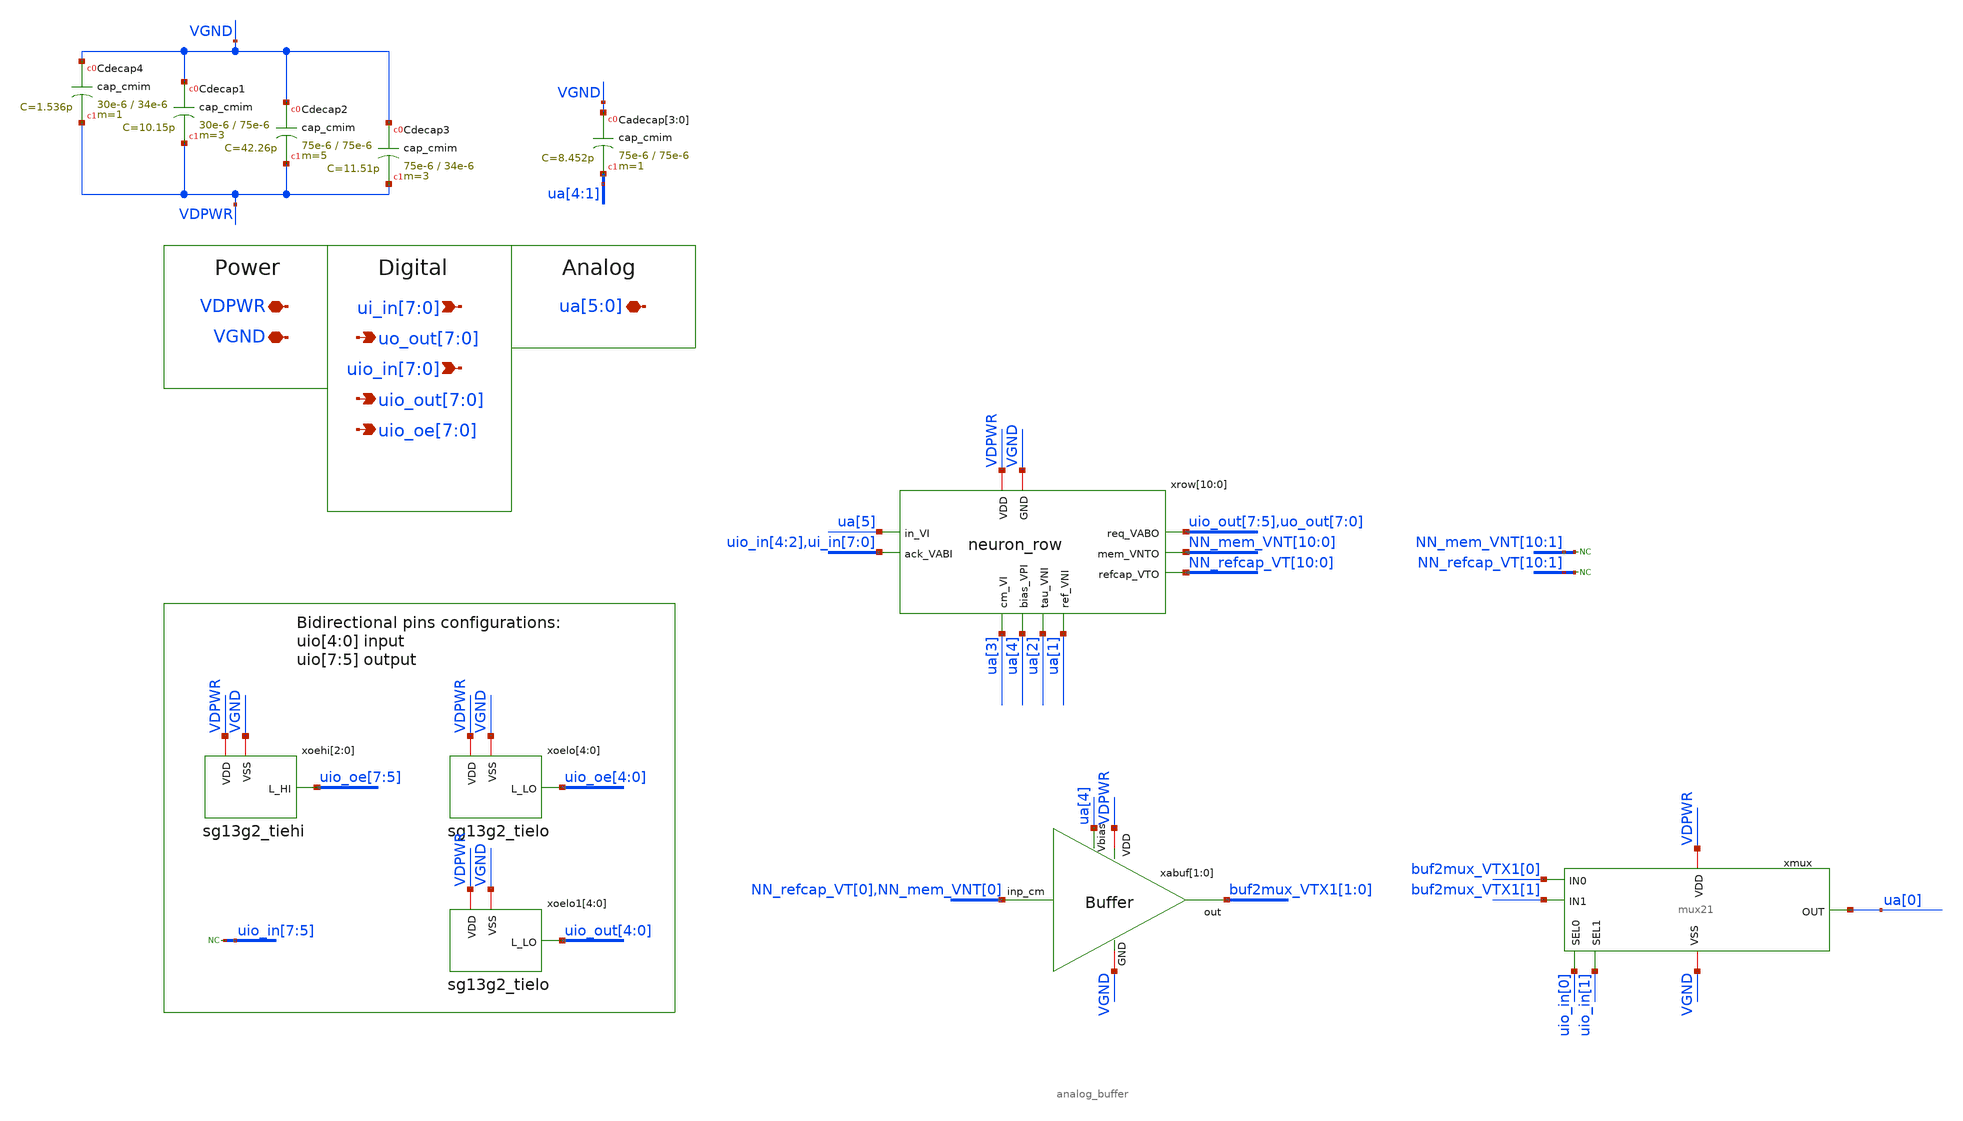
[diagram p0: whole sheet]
** sch_path: xschem/chip_top.sch
**.subckt chip_top VDPWR VGND
*+ ui_in[7],ui_in[6],ui_in[5],ui_in[4],ui_in[3],ui_in[2],ui_in[1],ui_in[0] uo_out[7],uo_out[6],uo_out[5],uo_out[4],uo_out[3],uo_out[2],uo_out[1],uo_out[0]
*+ uio_in[7],uio_in[6],uio_in[5],uio_in[4],uio_in[3],uio_in[2],uio_in[1],uio_in[0] uio_out[7],uio_out[6],uio_out[5],uio_out[4],uio_out[3],uio_out[2],uio_out[1],uio_out[0]
*+ uio_oe[7],uio_oe[6],uio_oe[5],uio_oe[4],uio_oe[3],uio_oe[2],uio_oe[1],uio_oe[0] ua[5],ua[4],ua[3],ua[2],ua[1],ua[0]
*.iopin VDPWR
*.iopin VGND
*.ipin ui_in[7],ui_in[6],ui_in[5],ui_in[4],ui_in[3],ui_in[2],ui_in[1],ui_in[0]
*.opin uo_out[7],uo_out[6],uo_out[5],uo_out[4],uo_out[3],uo_out[2],uo_out[1],uo_out[0]
*.ipin uio_in[7],uio_in[6],uio_in[5],uio_in[4],uio_in[3],uio_in[2],uio_in[1],uio_in[0]
*.opin uio_out[7],uio_out[6],uio_out[5],uio_out[4],uio_out[3],uio_out[2],uio_out[1],uio_out[0]
*.opin uio_oe[7],uio_oe[6],uio_oe[5],uio_oe[4],uio_oe[3],uio_oe[2],uio_oe[1],uio_oe[0]
*.iopin ua[5],ua[4],ua[3],ua[2],ua[1],ua[0]
xrow[10] VDPWR VGND ua[4] ua[5] NN_mem_VNT[10] ua[3] ua[2] uio_out[7] ua[1] NN_refcap_VT[10]
+ uio_in[4] neuron_row
xrow[9] VDPWR VGND ua[4] ua[5] NN_mem_VNT[9] ua[3] ua[2] uio_out[6] ua[1] NN_refcap_VT[9] uio_in[3]
+ neuron_row
xrow[8] VDPWR VGND ua[4] ua[5] NN_mem_VNT[8] ua[3] ua[2] uio_out[5] ua[1] NN_refcap_VT[8] uio_in[2]
+ neuron_row
xrow[7] VDPWR VGND ua[4] ua[5] NN_mem_VNT[7] ua[3] ua[2] uo_out[7] ua[1] NN_refcap_VT[7] ui_in[7]
+ neuron_row
xrow[6] VDPWR VGND ua[4] ua[5] NN_mem_VNT[6] ua[3] ua[2] uo_out[6] ua[1] NN_refcap_VT[6] ui_in[6]
+ neuron_row
xrow[5] VDPWR VGND ua[4] ua[5] NN_mem_VNT[5] ua[3] ua[2] uo_out[5] ua[1] NN_refcap_VT[5] ui_in[5]
+ neuron_row
xrow[4] VDPWR VGND ua[4] ua[5] NN_mem_VNT[4] ua[3] ua[2] uo_out[4] ua[1] NN_refcap_VT[4] ui_in[4]
+ neuron_row
xrow[3] VDPWR VGND ua[4] ua[5] NN_mem_VNT[3] ua[3] ua[2] uo_out[3] ua[1] NN_refcap_VT[3] ui_in[3]
+ neuron_row
xrow[2] VDPWR VGND ua[4] ua[5] NN_mem_VNT[2] ua[3] ua[2] uo_out[2] ua[1] NN_refcap_VT[2] ui_in[2]
+ neuron_row
xrow[1] VDPWR VGND ua[4] ua[5] NN_mem_VNT[1] ua[3] ua[2] uo_out[1] ua[1] NN_refcap_VT[1] ui_in[1]
+ neuron_row
xrow[0] VDPWR VGND ua[4] ua[5] NN_mem_VNT[0] ua[3] ua[2] uo_out[0] ua[1] NN_refcap_VT[0] ui_in[0]
+ neuron_row
xabuf[1] NN_refcap_VT[0] VDPWR ua[4] buf2mux_VTX1[1] VGND analog_buffer
xabuf[0] NN_mem_VNT[0] VDPWR ua[4] buf2mux_VTX1[0] VGND analog_buffer
xmux VDPWR VGND buf2mux_VTX1[0] buf2mux_VTX1[1] uio_in[0] uio_in[1] ua[0] mux21
xoehi[2] VDPWR VGND uio_oe[7] sg13g2_tiehi
xoehi[1] VDPWR VGND uio_oe[6] sg13g2_tiehi
xoehi[0] VDPWR VGND uio_oe[5] sg13g2_tiehi
xoelo[4] VDPWR VGND uio_oe[4] sg13g2_tielo
xoelo[3] VDPWR VGND uio_oe[3] sg13g2_tielo
xoelo[2] VDPWR VGND uio_oe[2] sg13g2_tielo
xoelo[1] VDPWR VGND uio_oe[1] sg13g2_tielo
xoelo[0] VDPWR VGND uio_oe[0] sg13g2_tielo
xoelo1[4] VDPWR VGND uio_out[4] sg13g2_tielo
xoelo1[3] VDPWR VGND uio_out[3] sg13g2_tielo
xoelo1[2] VDPWR VGND uio_out[2] sg13g2_tielo
xoelo1[1] VDPWR VGND uio_out[1] sg13g2_tielo
xoelo1[0] VDPWR VGND uio_out[0] sg13g2_tielo
* noconn uio_in[7:5]
* noconn NN_mem_VNT[10:1]
* noconn NN_refcap_VT[10:1]
XCadecap[3] VGND ua[4] cap_cmim w=75e-6 l=75e-6 m=1 mm_ok=1
XCadecap[2] VGND ua[3] cap_cmim w=75e-6 l=75e-6 m=1 mm_ok=1
XCadecap[1] VGND ua[2] cap_cmim w=75e-6 l=75e-6 m=1 mm_ok=1
XCadecap[0] VGND ua[1] cap_cmim w=75e-6 l=75e-6 m=1 mm_ok=1
XCdecap2 VGND VDPWR cap_cmim w=75e-6 l=75e-6 m=5 mm_ok=1
XCdecap1 VGND VDPWR cap_cmim w=30e-6 l=75e-6 m=3 mm_ok=1
XCdecap3 VGND VDPWR cap_cmim w=75e-6 l=34e-6 m=3 mm_ok=1
XCdecap4 VGND VDPWR cap_cmim w=30e-6 l=34e-6 m=1 mm_ok=1
**.ends
.end
